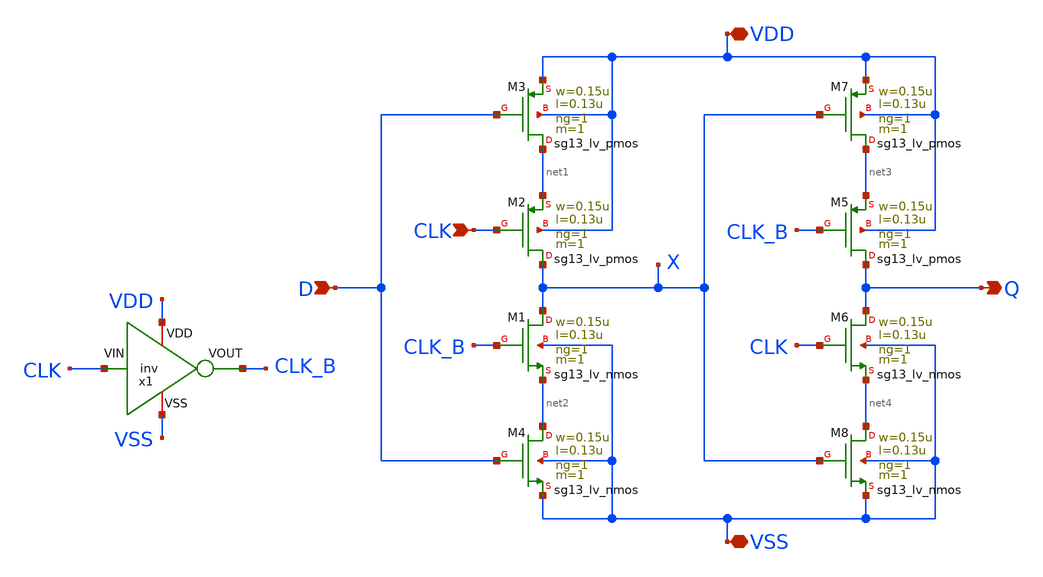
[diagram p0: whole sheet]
** sch_path: design/blocks-std-custom/reg/schematic/reg.sch
**.subckt reg D Q VDD VSS CLK
*.ipin D
*.opin Q
*.iopin VDD
*.iopin VSS
*.ipin CLK
XM2 X CLK net1 VDD sg13_lv_pmos w=0.15u l=0.13u ng=1 m=1 mm_ok=1
XM1 X CLK_B net2 VSS sg13_lv_nmos w=0.15u l=0.13u ng=1 m=1 mm_ok=1
XM3 net1 D VDD VDD sg13_lv_pmos w=0.15u l=0.13u ng=1 m=1 mm_ok=1
XM4 net2 D VSS VSS sg13_lv_nmos w=0.15u l=0.13u ng=1 m=1 mm_ok=1
XM5 Q CLK_B net3 VDD sg13_lv_pmos w=0.15u l=0.13u ng=1 m=1 mm_ok=1
XM6 Q CLK net4 VSS sg13_lv_nmos w=0.15u l=0.13u ng=1 m=1 mm_ok=1
XM7 net3 X VDD VDD sg13_lv_pmos w=0.15u l=0.13u ng=1 m=1 mm_ok=1
XM8 net4 X VSS VSS sg13_lv_nmos w=0.15u l=0.13u ng=1 m=1 mm_ok=1
x1 VDD CLK_B CLK VSS inv
**.ends
.end
